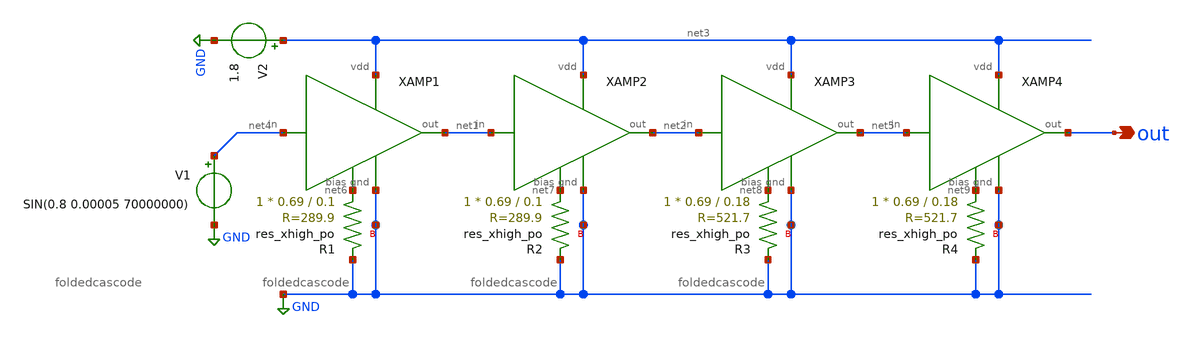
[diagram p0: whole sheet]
** sch_path: xschem/lna/lna4stage.sch
**.subckt lna4stage out
*.opin out
XAMP1 net4 GND net1 net3 net6 foldedcascode
XAMP2 net1 GND net2 net3 net7 foldedcascode
XAMP3 net2 GND net5 net3 net8 foldedcascode
V1 net4 GND SIN(0.8 0.00005 70000000)
V2 net3 GND 1.8
XAMP4 net5 GND out net3 net9 foldedcascode
XR1 net6 GND GND sky130_fd_pr__res_xhigh_po W=0.69 L=0.1 mult=1 m=1
XR2 net7 GND GND sky130_fd_pr__res_xhigh_po W=0.69 L=0.1 mult=1 m=1
XR3 net8 GND GND sky130_fd_pr__res_xhigh_po W=0.69 L=0.18 mult=1 m=1
XR4 net9 GND GND sky130_fd_pr__res_xhigh_po W=0.69 L=0.18 mult=1 m=1
**** begin user architecture code


.lib /foss/pdk/sky130A/libs.tech/ngspice/sky130.lib.spice tt
.control
	** dc V1 0.769 3.769 0.01
	** dc V2 0 3 0.01
        ** SIN(0.9 0.00001 70000000)
	tran 0.0000000001 0.0000001
.endc
.save all


 ** manual skywater pdks install (with patches applied)
* .lib $::SKYWATER_MODELS/models/sky130.lib.spice tt

** opencircuitdesign pdks install
.lib /foss/pdk/sky130A/libs.tech/ngspice/sky130.lib.spice tt

.param mc_mm_switch=0
.param mc_pr_switch=0

**** end user architecture code
**.ends
.GLOBAL GND
.end
